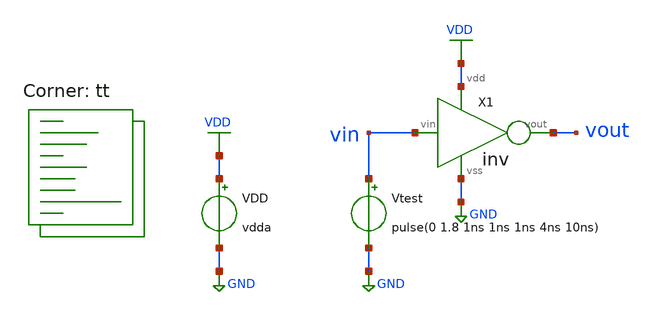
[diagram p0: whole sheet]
** sch_path: xsch/tb/tb_inv_tran.sch
**.subckt tb_inv_tran
X1 vin vout VDD GND inv
Vtest vin GND pulse(0 1.8 1ns 1ns 1ns 4ns 10ns)
VDD VDD GND vdda
**** begin user architecture code


.tran 0.01n 1u


.lib $::SKYWATER_MODELS/sky130.lib.spice tt


.save all




.param vdda=1.8




.control
	set wr_vecnames
	set wr_singlescale

	let mc_runs = 10
	let run = 1

	dowhile run <= mc_runs
		dc Vtest 0 1.8 0.01
		wrdata inverter{$&run}.raw v(vout)
		reset
		let run = run + 1
	end
.endc


**** end user architecture code
**.ends
.GLOBAL VDD
.GLOBAL GND
.end
